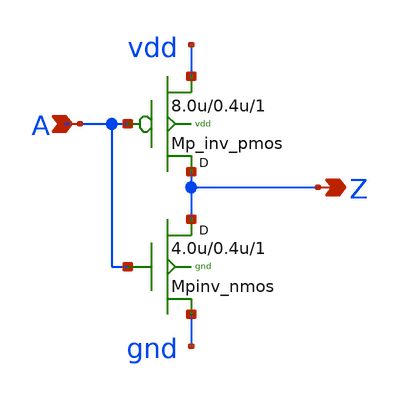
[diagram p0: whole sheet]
** sch_path: sram_2_16_scn4m/pinv_6.sch
**.subckt pinv_6 A Z
*.ipin A
*.opin Z
Mpinv_nmos Z A gnd gnd n w=4.0u l=0.4u m=1
Mp_inv_pmos Z A vdd vdd p w=8.0u l=0.4u m=1
**.ends
.end
